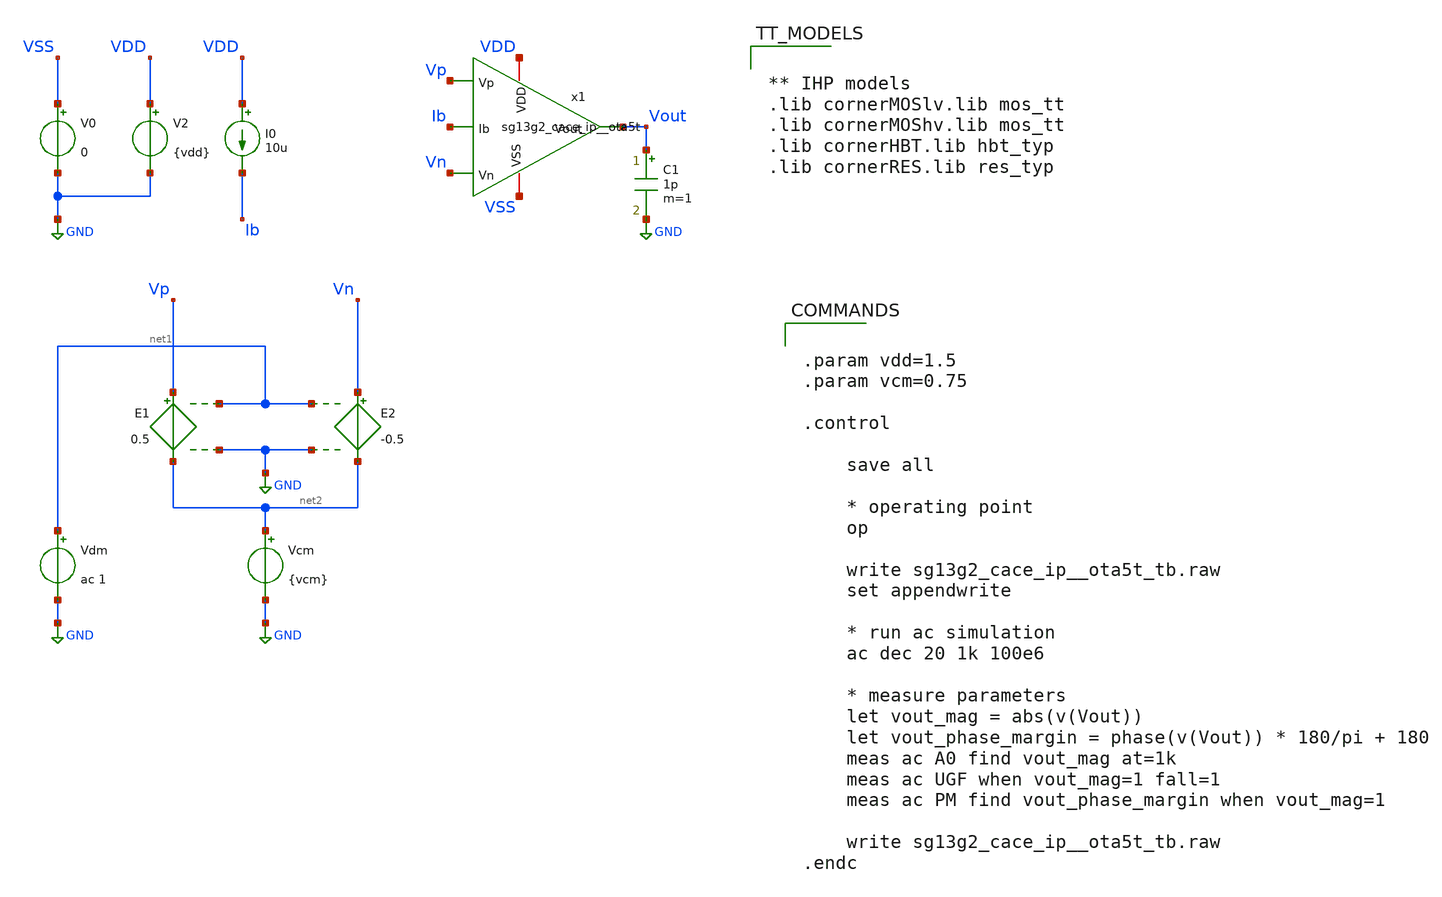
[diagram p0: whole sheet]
** sch_path: examples/sg13g2_cace_ip__ota5t/xschem/sg13g2_cace_ip__ota5t_tb.sch
**.subckt sg13g2_cace_ip__ota5t_tb
I0 VDD Ib 10u
C1 Vout GND 1p m=1
x1 Vp Vn Vout VDD VSS Ib sg13g2_cace_ip__ota5t
V0 VSS GND 0
V2 VDD GND {vdd}
E1 Vp net2 net1 GND 0.5
E2 Vn net2 net1 GND -0.5
Vdm net1 GND ac 1
Vcm net2 GND {vcm}
**** begin user architecture code


.param vdd=1.5
.param vcm=0.75

.control

    save all

    * operating point
    op

    write sg13g2_cace_ip__ota5t_tb.raw
    set appendwrite

    * run ac simulation
    ac dec 20 1k 100e6

    * measure parameters
    let vout_mag = abs(v(Vout))
    let vout_phase_margin = phase(v(Vout)) * 180/pi + 180
    meas ac A0 find vout_mag at=1k
    meas ac UGF when vout_mag=1 fall=1
    meas ac PM find vout_phase_margin when vout_mag=1

    write sg13g2_cace_ip__ota5t_tb.raw
.endc




** IHP models
.lib cornerMOSlv.lib mos_tt
.lib cornerMOShv.lib mos_tt
.lib cornerHBT.lib hbt_typ
.lib cornerRES.lib res_typ


**** end user architecture code
**.ends

* expanding   symbol:  sg13g2_cace_ip__ota5t.sym # of pins=6
** sym_path: examples/sg13g2_cace_ip__ota5t/xschem/sg13g2_cace_ip__ota5t.sym
** sch_path: examples/sg13g2_cace_ip__ota5t/xschem/sg13g2_cace_ip__ota5t.sch
.subckt sg13g2_cace_ip__ota5t Vp Vn Vout VDD VSS Ib
*.ipin Vp
*.ipin Vn
*.opin Vout
*.iopin VDD
*.iopin VSS
*.ipin Ib
XM10 node Ib VSS VSS sg13_lv_nmos w=2u l=1u ng=2 m=1 mm_ok=1
XM11 Vout net1 VDD VDD sg13_lv_pmos w=2u l=1u ng=2 m=1 mm_ok=1
XM1 Ib Ib VSS VSS sg13_lv_nmos w=2u l=1u ng=2 m=1 mm_ok=1
XM2 net1 net1 VDD VDD sg13_lv_pmos w=2u l=1u ng=2 m=1 mm_ok=1
XM3 Vout Vn node VSS sg13_lv_nmos w=20u l=0.5u ng=4 m=1 mm_ok=1
XM4 net1 Vp node VSS sg13_lv_nmos w=20u l=0.5u ng=4 m=1 mm_ok=1
.ends

.GLOBAL GND
.end
